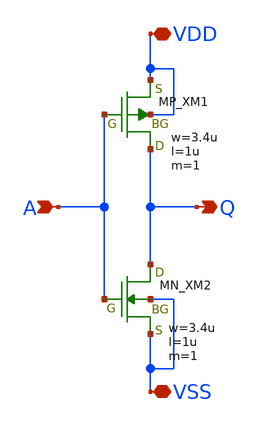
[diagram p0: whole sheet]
** sch_path: member_project/inverter/ichiken/Miyamoto_sprzk_naoyuki/inverter_Miyamoto_sprzk_naoyuki.sch
**.subckt inverter_Miyamoto_sprzk_naoyuki A VDD Q VSS
*.ipin A
*.iopin VDD
*.opin Q
*.iopin VSS
XM1 Q A VDD VDD PMOS w=3.4u l=1u as=0 ad=0 ps=0 pd=0 nrd=0 nrs=0 m=1
XM2 Q A VSS VSS NMOS w=3.4u l=1u as=0 ad=0 ps=0 pd=0 nrd=0 nrs=0 m=1
**.ends
.end
